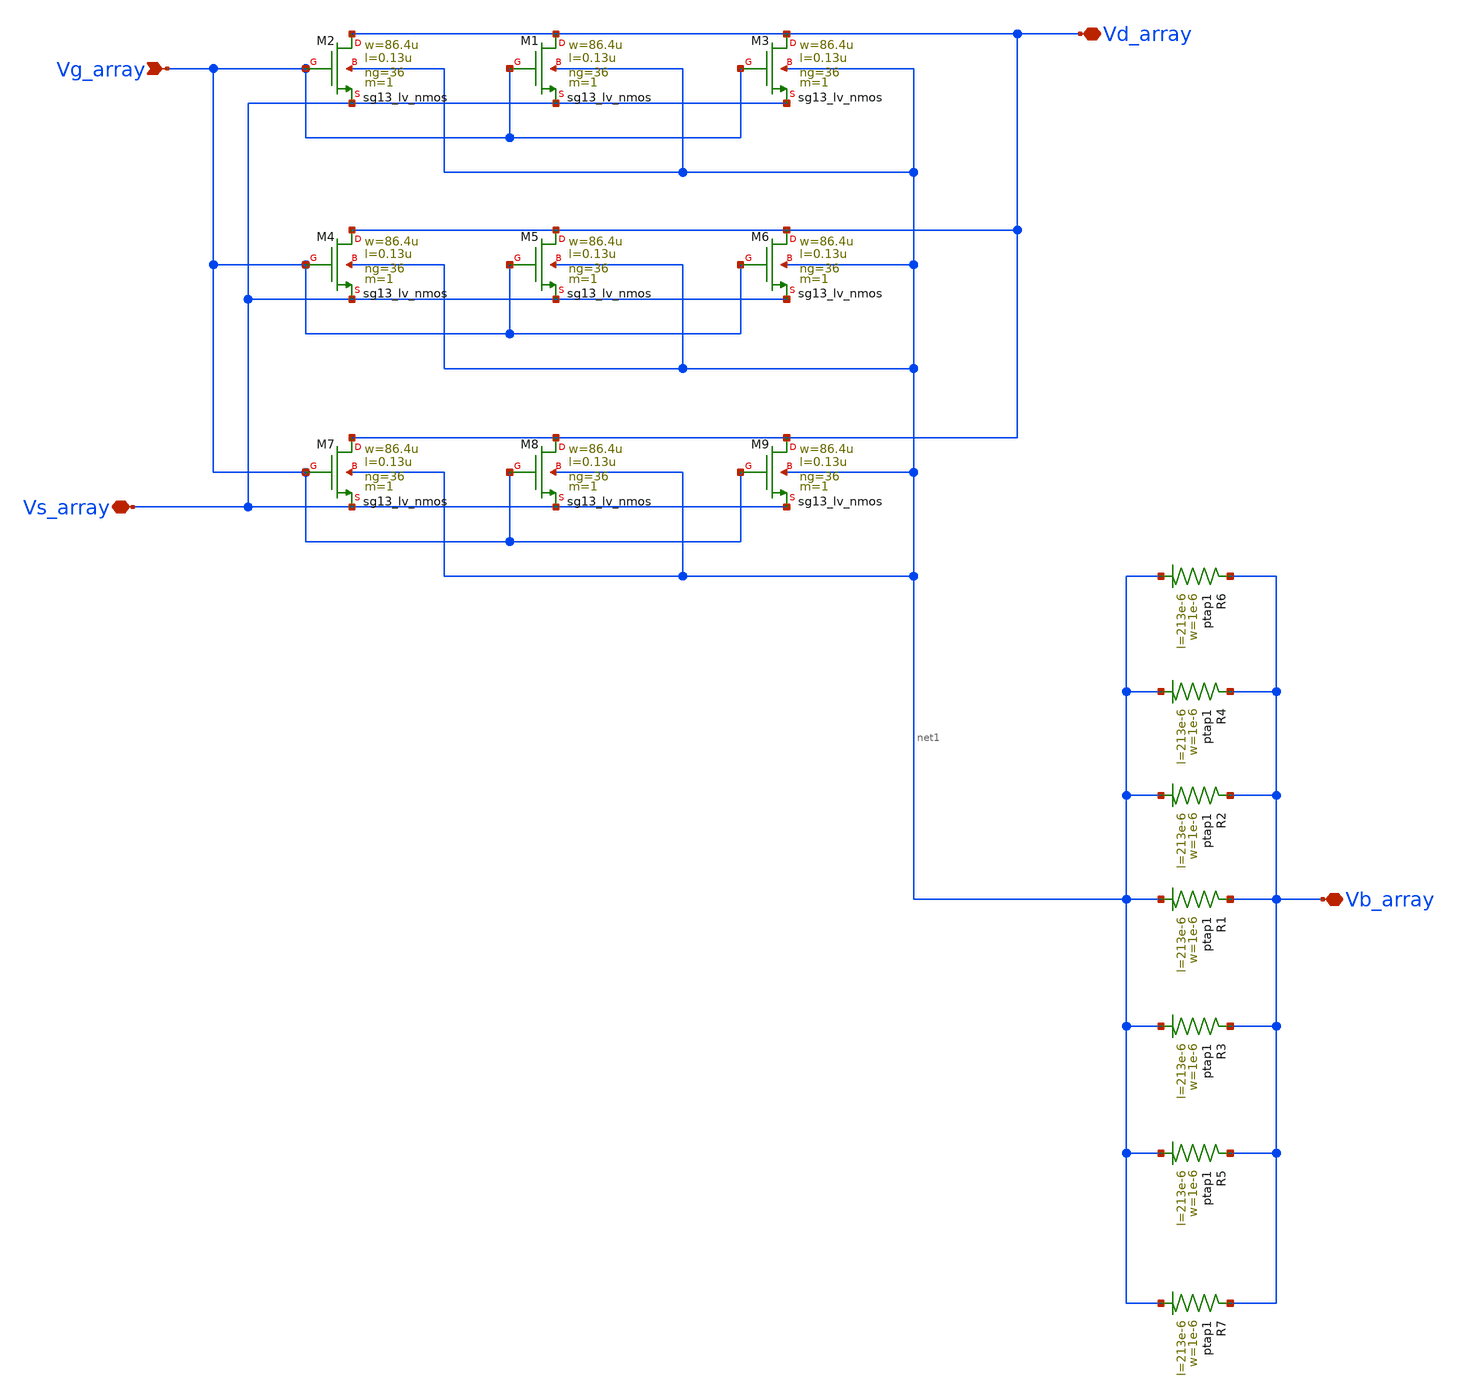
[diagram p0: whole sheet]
** sch_path: Layouts/PMOS/nmos_array.sch
**.subckt nmos_array Vd_array Vg_array Vs_array Vb_array
*.iopin Vd_array
*.ipin Vg_array
*.iopin Vs_array
*.iopin Vb_array
XM2 Vd_array Vg_array Vs_array net1 sg13_lv_nmos w=86.4u l=0.13u ng=36 m=1 mm_ok=1
XR2 Vb_array net1 ptap1 R=1.529 w=1e-6 l=213e-6
XM1 Vd_array Vg_array Vs_array net1 sg13_lv_nmos w=86.4u l=0.13u ng=36 m=1 mm_ok=1
XM3 Vd_array Vg_array Vs_array net1 sg13_lv_nmos w=86.4u l=0.13u ng=36 m=1 mm_ok=1
XM4 Vd_array Vg_array Vs_array net1 sg13_lv_nmos w=86.4u l=0.13u ng=36 m=1 mm_ok=1
XM5 Vd_array Vg_array Vs_array net1 sg13_lv_nmos w=86.4u l=0.13u ng=36 m=1 mm_ok=1
XM6 Vd_array Vg_array Vs_array net1 sg13_lv_nmos w=86.4u l=0.13u ng=36 m=1 mm_ok=1
XM7 Vd_array Vg_array Vs_array net1 sg13_lv_nmos w=86.4u l=0.13u ng=36 m=1 mm_ok=1
XM8 Vd_array Vg_array Vs_array net1 sg13_lv_nmos w=86.4u l=0.13u ng=36 m=1 mm_ok=1
XM9 Vd_array Vg_array Vs_array net1 sg13_lv_nmos w=86.4u l=0.13u ng=36 m=1 mm_ok=1
XR1 Vb_array net1 ptap1 R=1.529 w=1e-6 l=213e-6
XR3 Vb_array net1 ptap1 R=1.529 w=1e-6 l=213e-6
XR4 Vb_array net1 ptap1 R=1.529 w=1e-6 l=213e-6
XR5 Vb_array net1 ptap1 R=1.529 w=1e-6 l=213e-6
XR6 Vb_array net1 ptap1 R=1.529 w=1e-6 l=213e-6
XR7 Vb_array net1 ptap1 R=1.529 w=1e-6 l=213e-6
**.ends
.end
